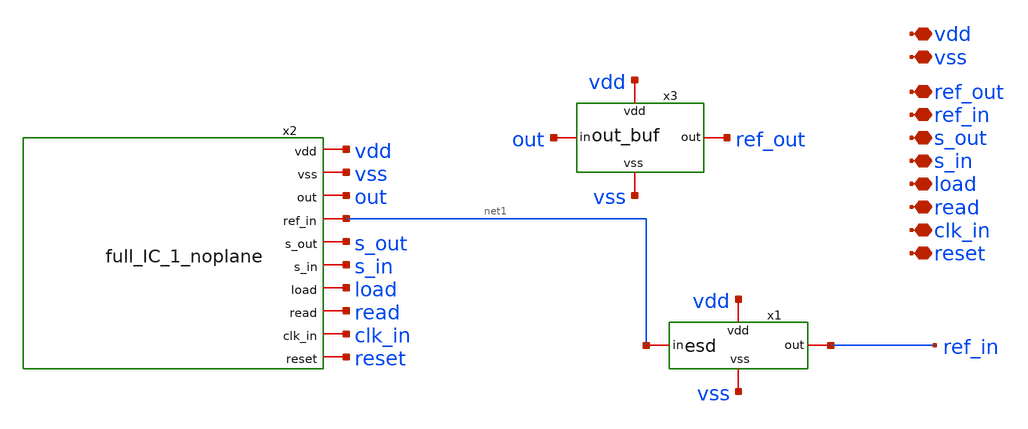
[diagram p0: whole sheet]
** sch_path: xschem/complete_wrapper_noplane.sch
**.subckt complete_wrapper_noplane vss vdd s_out s_in reset ref_out ref_in read load clk_in
*.iopin vss
*.iopin vdd
*.iopin s_out
*.iopin s_in
*.iopin reset
*.iopin ref_out
*.iopin ref_in
*.iopin read
*.iopin load
*.iopin clk_in
x3 vdd ref_out out vss out_buf
x1 net1 vdd vss ref_in esd
x2 vdd vss net1 s_out s_in load read clk_in reset out full_IC_1_noplane
**.ends
.end
